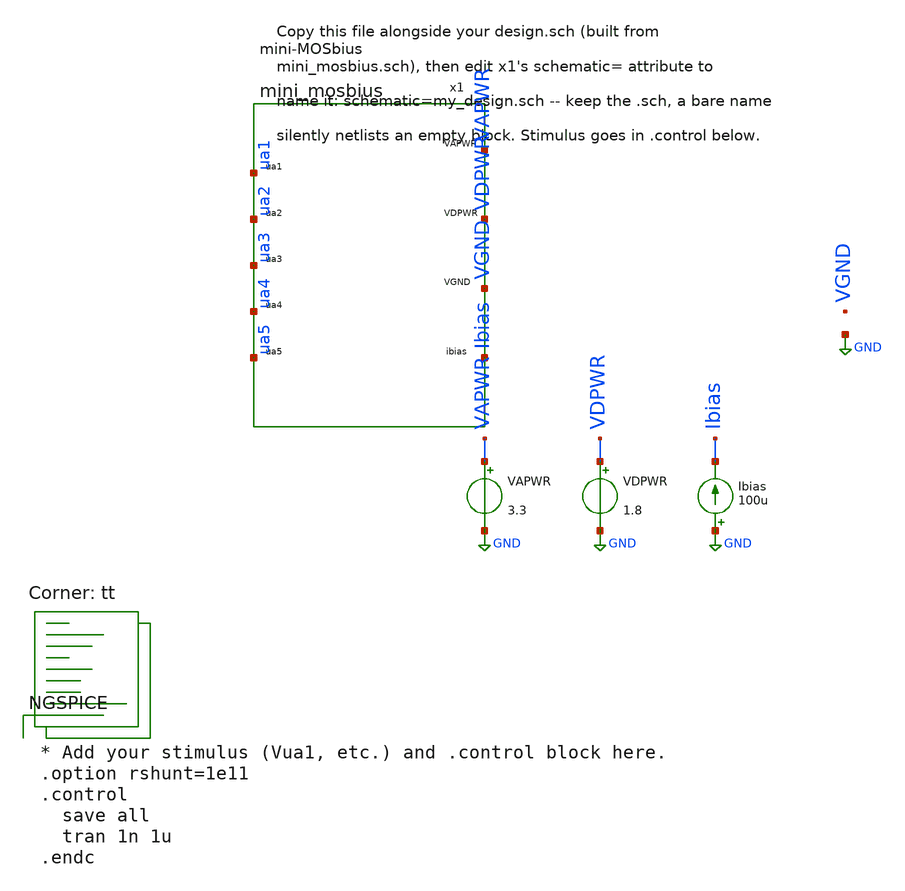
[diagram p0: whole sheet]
** sch_path: xschem/mosbius_lib/tb_template.sch
**.subckt tb_template
x1 Ibias ua1 ua2 ua3 ua4 ua5 VAPWR VDPWR VGND mini_mosbius
VAPWR VAPWR GND 3.3
VDPWR VDPWR GND 1.8
Ibias GND Ibias 100u
**** begin user architecture code
.lib $::SKYWATER_MODELS/sky130.lib.spice tt


* Add your stimulus (Vua1, etc.) and .control block here.
.option rshunt=1e11
.control
  save all
  tran 1n 1u
.endc


**** end user architecture code
**.ends

* expanding   symbol:  mini_mosbius.sym # of pins=9
** sym_path: xschem/mosbius_lib/mini_mosbius.sym
** sch_path: xschem/mosbius_lib/mini_mosbius.sch
.subckt mini_mosbius ibias ua1 ua2 ua3 ua4 ua5 VAPWR VDPWR VGND
*.iopin ibias
*.iopin ua1
*.iopin ua2
*.iopin ua3
*.iopin ua4
*.iopin ua5
*.iopin VAPWR
*.iopin VDPWR
*.iopin VGND
.ends

.GLOBAL GND
.end
